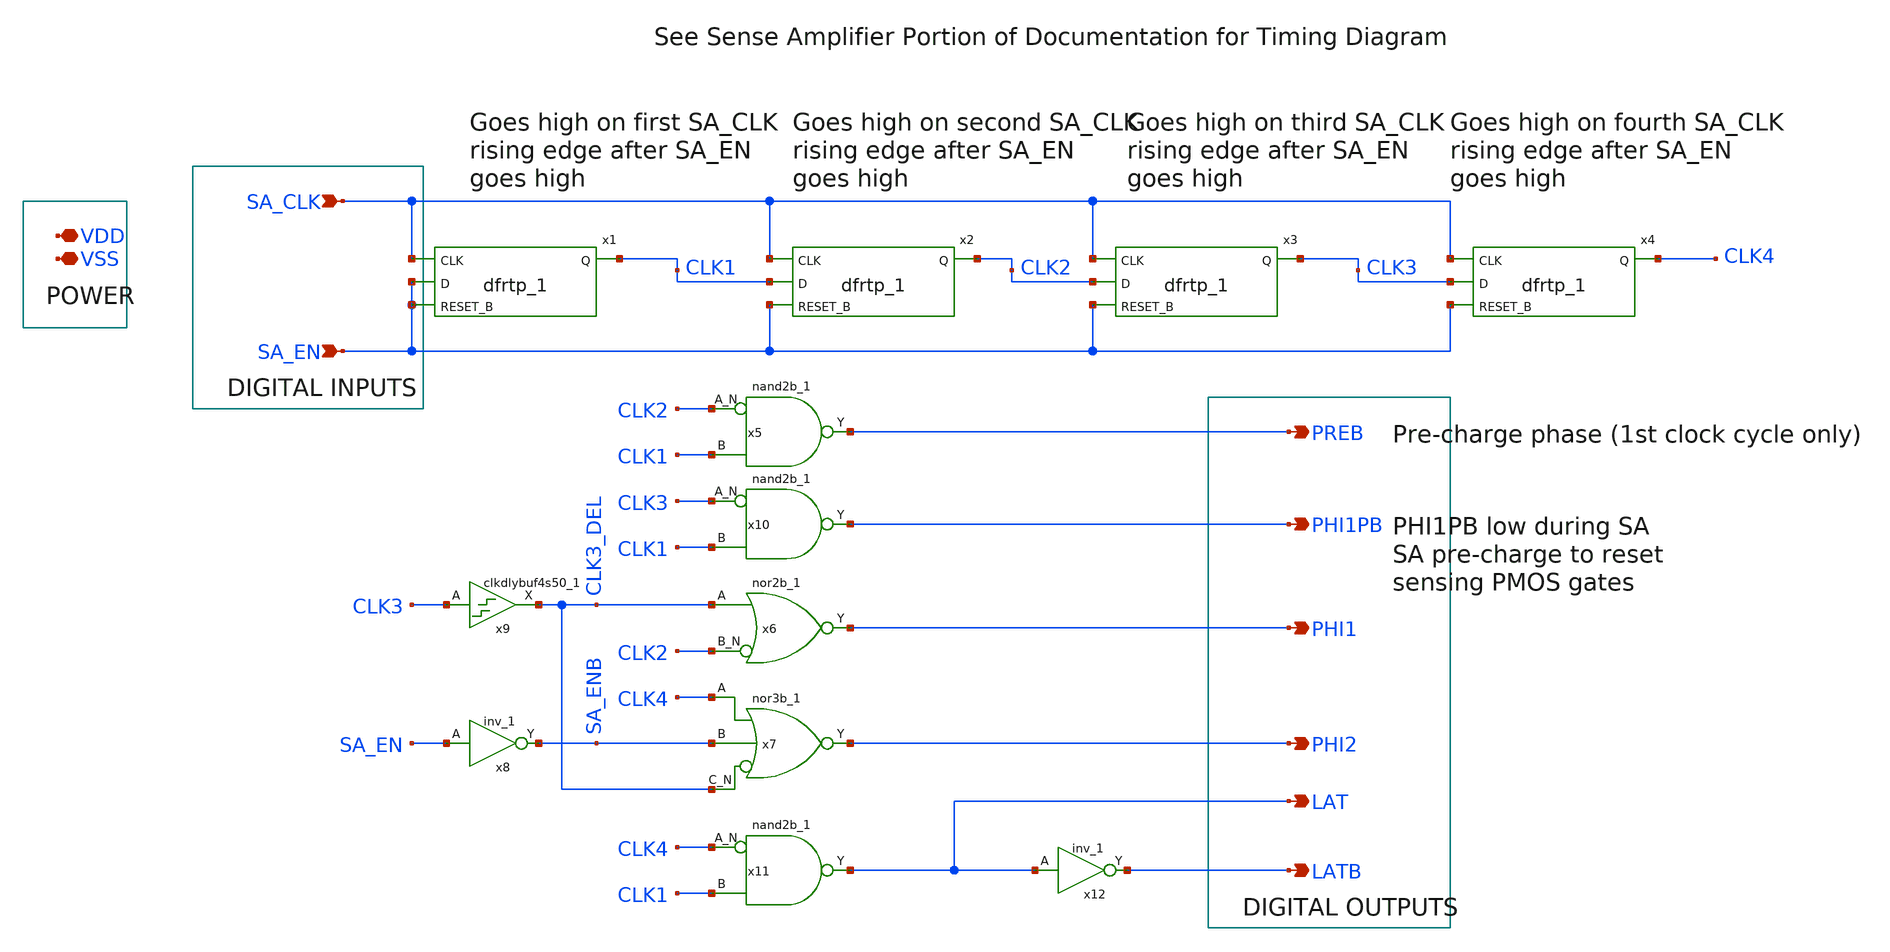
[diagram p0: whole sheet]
** sch_path: BL_Read_Interface/rram_read_csa_clk.sch
**.subckt rram_read_csa_clk SA_EN SA_CLK VDD VSS PREB PHI1PB PHI1 PHI2 LATB LAT
*.ipin SA_EN
*.ipin SA_CLK
*.iopin VDD
*.iopin VSS
*.opin PREB
*.opin PHI1PB
*.opin PHI1
*.opin PHI2
*.opin LATB
*.opin LAT
x1 SA_CLK SA_EN SA_EN VSS VSS VDD VDD CLK1 sky130_fd_sc_hd__dfrtp_1
x2 SA_CLK CLK1 SA_EN VSS VSS VDD VDD CLK2 sky130_fd_sc_hd__dfrtp_1
x3 SA_CLK CLK2 SA_EN VSS VSS VDD VDD CLK3 sky130_fd_sc_hd__dfrtp_1
x4 SA_CLK CLK3 SA_EN VSS VSS VDD VDD CLK4 sky130_fd_sc_hd__dfrtp_1
x5 CLK2 CLK1 VSS VSS VDD VDD PREB sky130_fd_sc_hd__nand2b_1
x6 CLK3_DEL CLK2 VSS VSS VDD VDD PHI1 sky130_fd_sc_hd__nor2b_1
x7 CLK4 SA_ENB CLK3_DEL VSS VSS VDD VDD PHI2 sky130_fd_sc_hd__nor3b_1
x8 SA_EN VSS VSS VDD VDD SA_ENB sky130_fd_sc_hd__inv_1
x9 CLK3 VSS VSS VDD VDD CLK3_DEL sky130_fd_sc_hd__clkdlybuf4s50_1
x10 CLK3 CLK1 VSS VSS VDD VDD PHI1PB sky130_fd_sc_hd__nand2b_1
x11 CLK4 CLK1 VSS VSS VDD VDD LAT sky130_fd_sc_hd__nand2b_1
x12 LAT VSS VSS VDD VDD LATB sky130_fd_sc_hd__inv_1
**.ends
.end
